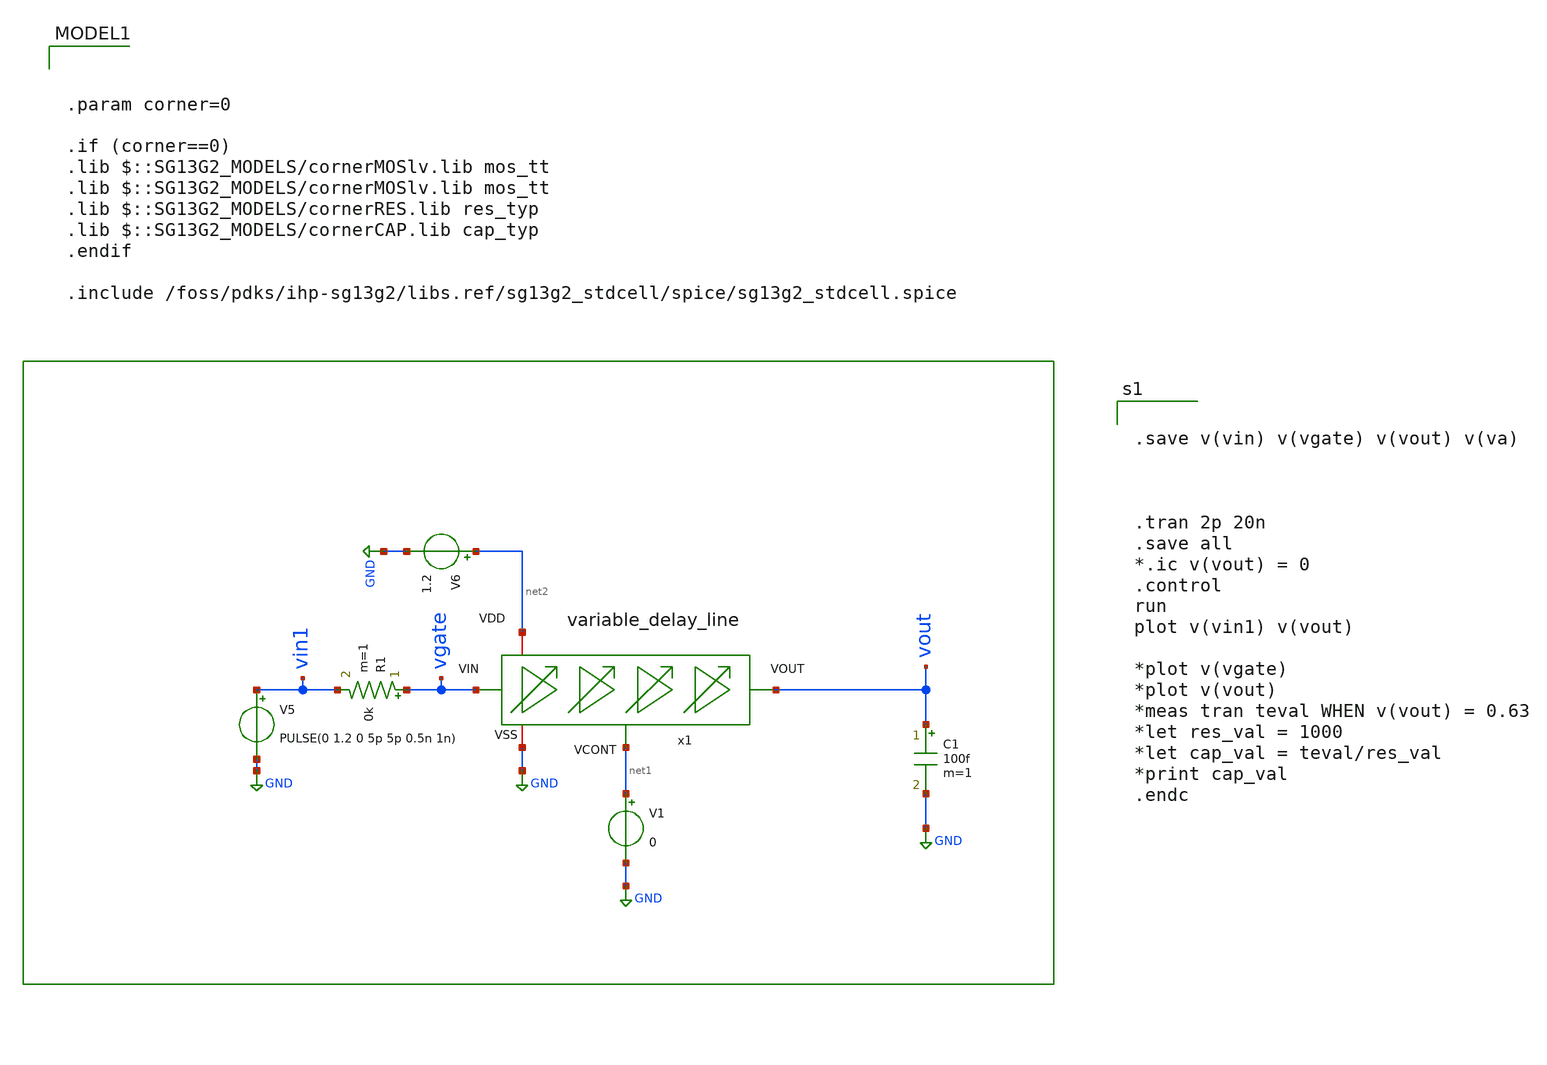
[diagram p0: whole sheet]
** sch_path: xschem/delay_variable_line/tb_variable_delay_line.sch
* IHP-GmbH/IHP-Open-PDK/ihp-sg13g2/libs.tech/xschem/sg13g2_stdcells/sg13g2_dlygate4sd2_1.sch:
* Copyright 2023 IHP PDK Authors
* Licensed under the Apache License, Version 2.0 (the "License");
**.subckt tb_variable_delay_line
x1 net2 GND net1 vout vgate variable_delay_line
C1 vout GND 100f m=1
V1 net1 GND 0
R1 vgate vin1 0k m=1
V5 vin1 GND PULSE(0 1.2 0 5p 5p 0.5n 1n)
V6 net2 GND 1.2
**** begin user architecture code


.save v(vin) v(vgate) v(vout) v(va)



.tran 2p 20n
.save all
*.ic v(vout) = 0
.control
run
plot v(vin1) v(vout)

*plot v(vgate)
*plot v(vout)
*meas tran teval WHEN v(vout) = 0.63
*let res_val = 1000
*let cap_val = teval/res_val
*print cap_val
.endc




.param corner=0

.if (corner==0)
.lib $::SG13G2_MODELS/cornerMOSlv.lib mos_tt
.lib $::SG13G2_MODELS/cornerMOSlv.lib mos_tt
.lib $::SG13G2_MODELS/cornerRES.lib res_typ
.lib $::SG13G2_MODELS/cornerCAP.lib cap_typ
.endif

.include /foss/pdks/ihp-sg13g2/libs.ref/sg13g2_stdcell/spice/sg13g2_stdcell.spice

**** end user architecture code
**.ends

* expanding   symbol:  /foss/designs/UNIC-CASS-Aug25/sch/delay_variable_line/variable_delay_line.sym
*+ # of pins=5
** sym_path: xschem/delay_variable_line/variable_delay_line.sym
** sch_path: xschem/delay_variable_line/variable_delay_line.sch
.subckt variable_delay_line VDD VSS VCONT VOUT VIN
*.iopin VSS
*.iopin VDD
*.ipin VIN
*.opin VOUT
*.ipin VCONT
x1 VDD VIN va VCONT VSS delay_variable
x2 VDD VSS va VOUT large_delay_vto1p1
.ends


* expanding   symbol:  /foss/designs/UNIC-CASS-Aug25/sch/delay_variable/delay_variable.sym # of
*+ pins=5
** sym_path: xschem/delay_variable/delay_variable.sym
** sch_path: xschem/delay_variable/delay_variable.sch
.subckt delay_variable VDD_D VIN_D VOUT_D VCONT_D VSS_D
*.iopin VSS_D
*.iopin VDD_D
*.opin VOUT_D
*.ipin VCONT_D
*.ipin VIN_D
XM3 net3 VCONT_D VSS_D VSS_D sg13_lv_nmos w=1u l=0.13u ng=1 m=1 mm_ok=1
XM5 net2 VCONT_D VSS_D VSS_D sg13_lv_nmos w=2u l=2u ng=1 m=1 mm_ok=1
XM4 net3 net3 VDD_D VDD_D sg13_lv_pmos w=2.24u l=0.13u ng=1 m=1 mm_ok=1
XM6 net1 net3 VDD_D VDD_D sg13_lv_pmos w=4u l=2u ng=1 m=1 mm_ok=1
XM7 VOUT_D VIN_D net1 VDD_D sg13_lv_pmos w=20u l=2u ng=4 m=1 mm_ok=1
XM8 VOUT_D VIN_D net2 VSS_D sg13_lv_nmos w=5u l=3u ng=1 m=1 mm_ok=1
.ends


* expanding   symbol:  /foss/designs/UNIC-CASS-Aug25/sch/large_delay_vto1p1/large_delay_vto1p1.sym #
*+ of pins=4
** sym_path: xschem/large_delay_vto1p1/large_delay_vto1p1.sym
** sch_path: xschem/large_delay_vto1p1/large_delay_vto1p1.sch
.subckt large_delay_vto1p1 VCC VSS VIN VOUT
*.iopin VIN
*.iopin VOUT
*.iopin VCC
*.iopin VSS
x1 VOUT VIN VCC VSS sg13g2_dlygate4sd2_1
x2 VOUT VIN VCC VSS sg13g2_dlygate4sd2_1
x3 VOUT VIN VCC VSS sg13g2_dlygate4sd2_1
x10 VOUT VIN VCC VSS sg13g2_dlygate4sd2_1
.ends


* expanding   symbol:  sg13g2_stdcells/sg13g2_dlygate4sd3_1.sym # of pins=2
** sym_path: sg13g2_stdcells/sg13g2_dlygate4sd3_1.sym
** sch_path: sg13g2_stdcells/sg13g2_dlygate4sd3_1.sch
.subckt sg13g2_dlygate4sd3_1 X A VDD VSS
*.ipin A
*.opin X
*.iopin VDD
*.iopin VSS
XM1 net3 A VSS VSS sg13_lv_nmos w=420.00n l=130.00n ng=1 m=1 mm_ok=1
XM2 net1 net3 VSS VSS sg13_lv_nmos w=420.00n l=500.0n ng=1 m=1 mm_ok=1
XM3 net2 net1 VSS VSS sg13_lv_nmos w=420.00n l=500.0n ng=1 m=1 mm_ok=1
XM4 X net2 VSS VSS sg13_lv_nmos w=740.00n l=130.00n ng=1 m=1 mm_ok=1
XM5 net3 A VDD VDD sg13_lv_pmos w=420.00n l=130.00n ng=1 m=1 mm_ok=1
XM6 net1 net3 VDD VDD sg13_lv_pmos w=1.000u l=500.0n ng=1 m=1 mm_ok=1
XM7 net2 net1 VDD VDD sg13_lv_pmos w=1.000u l=500.0n ng=1 m=1 mm_ok=1
XM8 X net2 VDD VDD sg13_lv_pmos w=1.12u l=130.00n ng=1 m=1 mm_ok=1
.ends


* expanding   symbol:  sg13g2_stdcells/sg13g2_dlygate4sd2_1.sym # of pins=2
** sym_path: sg13g2_stdcells/sg13g2_dlygate4sd2_1.sym
** sch_path: sg13g2_stdcells/sg13g2_dlygate4sd2_1.sch
.subckt sg13g2_dlygate4sd2_1 X A VDD VSS
*.ipin A
*.opin X
*.iopin VDD
*.iopin VSS
XM1 net2 A VSS VSS sg13_lv_nmos w=420.00n l=130.00n ng=1 m=1 mm_ok=1
XM2 net1 net2 VSS VSS sg13_lv_nmos w=420.00n l=180.00n ng=1 m=1 mm_ok=1
XM3 net3 net1 VSS VSS sg13_lv_nmos w=420.00n l=180.00n ng=1 m=1 mm_ok=1
XM4 X net3 VSS VSS sg13_lv_nmos w=740.00n l=130.00n ng=1 m=1 mm_ok=1
XM5 net2 A VDD VDD sg13_lv_pmos w=420.00n l=130.00n ng=1 m=1 mm_ok=1
XM6 net1 net2 VDD VDD sg13_lv_pmos w=1.000u l=250.00n ng=1 m=1 mm_ok=1
XM7 net3 net1 VDD VDD sg13_lv_pmos w=1.000u l=250.00n ng=1 m=1 mm_ok=1
XM8 X net3 VDD VDD sg13_lv_pmos w=1.12u l=130.00n ng=1 m=1 mm_ok=1
.ends

.GLOBAL GND
.end
